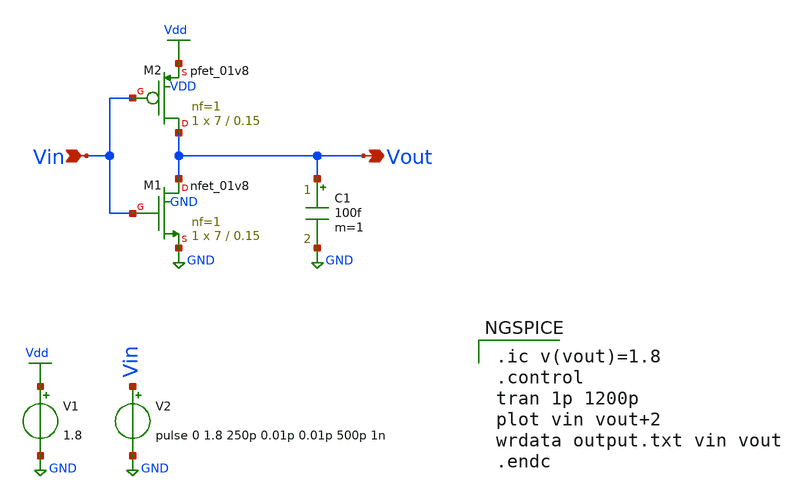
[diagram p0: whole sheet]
** sch_path: Circuiti/porta-not-ritardi.sch
**.subckt porta-not-ritardi Vin Vout
*.ipin Vin
*.opin Vout
XM1 Vout Vin GND GND sky130_fd_pr__nfet_01v8 L=0.15 W=7 nf=1 ad='int((nf+1)/2) * W/nf * 0.29' as='int((nf+2)/2) * W/nf * 0.29'
+ pd='2*int((nf+1)/2) * (W/nf + 0.29)' ps='2*int((nf+2)/2) * (W/nf + 0.29)' nrd='0.29 / W' nrs='0.29 / W'
+ sa=0 sb=0 sd=0 mult=1 m=1
V1 Vdd GND 1.8
XM2 Vout Vin Vdd VDD sky130_fd_pr__pfet_01v8 L=0.15 W=7 nf=1 ad='int((nf+1)/2) * W/nf * 0.29' as='int((nf+2)/2) * W/nf * 0.29'
+ pd='2*int((nf+1)/2) * (W/nf + 0.29)' ps='2*int((nf+2)/2) * (W/nf + 0.29)' nrd='0.29 / W' nrs='0.29 / W'
+ sa=0 sb=0 sd=0 mult=1 m=1
V2 Vin GND pulse 0 1.8 250p 0.01p 0.01p 500p 1n
C1 Vout GND 100f m=1
**** begin user architecture code


.lib /home/matteo/xschem_downloads/skywater-pdk/libraries/sky130_fd_pr_ngspice/latest/models/sky130.lib.spice tt

*.include /home/matteo/xschem_downloads/skywater-pdk/libraries/sky130_fd_pr_ngspice/latest/cells/nfet_01v8/sky130_fd_pr__nfet_01v8__tt.corner.spice

.param mc_mm_switch=0
.param mc_pr_switch=1



.ic v(vout)=1.8
.control
tran 1p 1200p
plot vin vout+2
wrdata output.txt vin vout
.endc


**** end user architecture code
**.ends
.GLOBAL Vdd
.GLOBAL GND
.end
